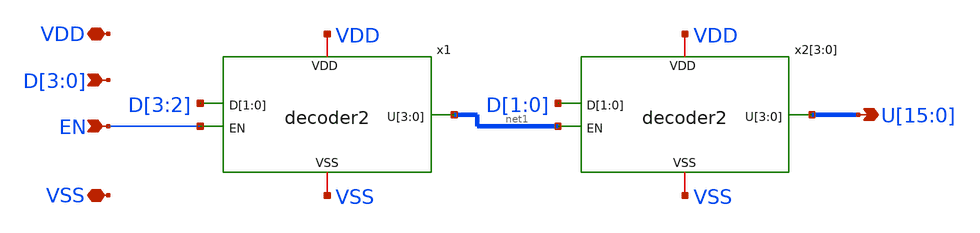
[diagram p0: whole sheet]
** sch_path: xschem/decoder4.sch
**.subckt decoder4 VDD VSS
*+ U[15],U[14],U[13],U[12],U[11],U[10],U[9],U[8],U[7],U[6],U[5],U[4],U[3],U[2],U[1],U[0] D[3],D[2],D[1],D[0] EN
*.iopin VDD
*.iopin VSS
*.opin U[15],U[14],U[13],U[12],U[11],U[10],U[9],U[8],U[7],U[6],U[5],U[4],U[3],U[2],U[1],U[0]
*.ipin D[3],D[2],D[1],D[0]
*.ipin EN
x1 VDD D[3] D[2] net1[3] net1[2] net1[1] net1[0] VSS EN decoder2
x2[3] VDD D[1] D[0] U[15] U[14] U[13] U[12] VSS net1[3] decoder2
x2[2] VDD D[1] D[0] U[11] U[10] U[9] U[8] VSS net1[2] decoder2
x2[1] VDD D[1] D[0] U[7] U[6] U[5] U[4] VSS net1[1] decoder2
x2[0] VDD D[1] D[0] U[3] U[2] U[1] U[0] VSS net1[0] decoder2
**.ends
.end
